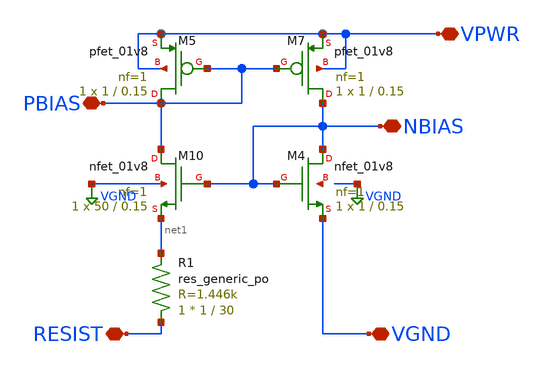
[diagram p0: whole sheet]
** sch_path: libs.ref/sky130_hilas_sc/xschem/sky130_hilas_Bootstrap01.sch
**.subckt sky130_hilas_Bootstrap01 VPWR NBIAS PBIAS VGND RESIST
*.iopin VPWR
*.iopin NBIAS
*.iopin PBIAS
*.iopin VGND
*.iopin RESIST
XM4 NBIAS NBIAS VGND net2 sky130_fd_pr__nfet_01v8 L=0.15 W=1 nf=1 ad='int((nf+1)/2) * W/nf * 0.29' as='int((nf+2)/2) * W/nf * 0.29'
+ pd='2*int((nf+1)/2) * (W/nf + 0.29)' ps='2*int((nf+2)/2) * (W/nf + 0.29)' nrd='0.29 / W' nrs='0.29 / W'
+ sa=0 sb=0 sd=0 mult=1 m=1
XM7 NBIAS PBIAS VPWR VPWR sky130_fd_pr__pfet_01v8 L=0.15 W=1 nf=1 ad='int((nf+1)/2) * W/nf * 0.29' as='int((nf+2)/2) * W/nf * 0.29'
+ pd='2*int((nf+1)/2) * (W/nf + 0.29)' ps='2*int((nf+2)/2) * (W/nf + 0.29)' nrd='0.29 / W' nrs='0.29 / W'
+ sa=0 sb=0 sd=0 mult=1 m=1
XM10 PBIAS NBIAS net1 VGND sky130_fd_pr__nfet_01v8 L=0.15 W=50 nf=1 ad='int((nf+1)/2) * W/nf * 0.29'
+ as='int((nf+2)/2) * W/nf * 0.29' pd='2*int((nf+1)/2) * (W/nf + 0.29)' ps='2*int((nf+2)/2) * (W/nf + 0.29)'
+ nrd='0.29 / W' nrs='0.29 / W' sa=0 sb=0 sd=0 mult=1 m=1
XM5 PBIAS PBIAS VPWR VPWR sky130_fd_pr__pfet_01v8 L=0.15 W=1 nf=1 ad='int((nf+1)/2) * W/nf * 0.29' as='int((nf+2)/2) * W/nf * 0.29'
+ pd='2*int((nf+1)/2) * (W/nf + 0.29)' ps='2*int((nf+2)/2) * (W/nf + 0.29)' nrd='0.29 / W' nrs='0.29 / W'
+ sa=0 sb=0 sd=0 mult=1 m=1
XR1 RESIST net1 sky130_fd_pr__res_generic_po W=1 L=30 m=1
**.ends
.GLOBAL VGND
.end
